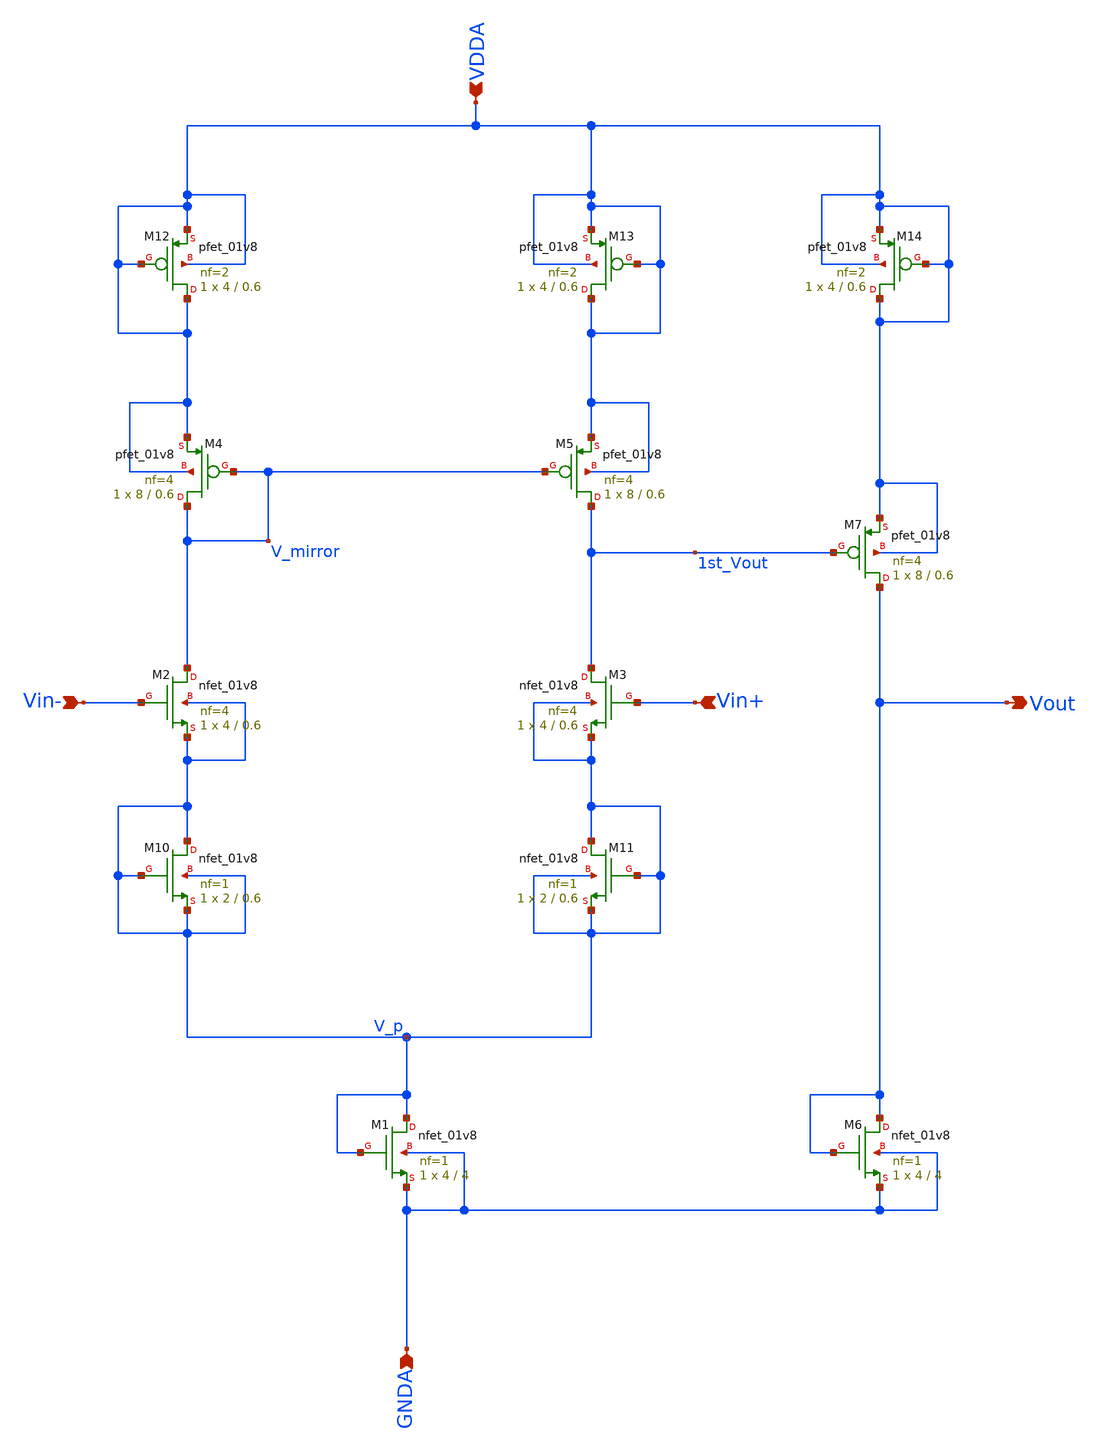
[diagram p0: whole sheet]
** sch_path: projects/bandgapref/xschem_ngspice/new_files/opamp_bandgap_dummy.sch
**.subckt opamp_bandgap_dummy Vin+ Vout Vin- GNDA VDDA
*.ipin Vin+
*.opin Vout
*.ipin Vin-
*.ipin GNDA
*.ipin VDDA
XM1 V_p V_p GNDA GNDA sky130_fd_pr__nfet_01v8 L=4 W=4 nf=1 ad='int((nf+1)/2) * W/nf * 0.29' as='int((nf+2)/2) * W/nf * 0.29'
+ pd='2*int((nf+1)/2) * (W/nf + 0.29)' ps='2*int((nf+2)/2) * (W/nf + 0.29)' nrd='0.29 / W' nrs='0.29 / W'
+ sa=0 sb=0 sd=0 mult=1 m=1
XM2 V_mirror Vin- V_p V_p sky130_fd_pr__nfet_01v8 L=0.6 W=4 nf=4 ad='int((nf+1)/2) * W/nf * 0.29' as='int((nf+2)/2) * W/nf * 0.29'
+ pd='2*int((nf+1)/2) * (W/nf + 0.29)' ps='2*int((nf+2)/2) * (W/nf + 0.29)' nrd='0.29 / W' nrs='0.29 / W'
+ sa=0 sb=0 sd=0 mult=1 m=1
XM3 1st_Vout Vin+ V_p V_p sky130_fd_pr__nfet_01v8 L=0.6 W=4 nf=4 ad='int((nf+1)/2) * W/nf * 0.29' as='int((nf+2)/2) * W/nf * 0.29'
+ pd='2*int((nf+1)/2) * (W/nf + 0.29)' ps='2*int((nf+2)/2) * (W/nf + 0.29)' nrd='0.29 / W' nrs='0.29 / W'
+ sa=0 sb=0 sd=0 mult=1 m=1
XM4 V_mirror V_mirror VDDA VDDA sky130_fd_pr__pfet_01v8 L=0.6 W=8 nf=4 ad='int((nf+1)/2) * W/nf * 0.29'
+ as='int((nf+2)/2) * W/nf * 0.29' pd='2*int((nf+1)/2) * (W/nf + 0.29)' ps='2*int((nf+2)/2) * (W/nf + 0.29)'
+ nrd='0.29 / W' nrs='0.29 / W' sa=0 sb=0 sd=0 mult=1 m=1
XM5 1st_Vout V_mirror VDDA VDDA sky130_fd_pr__pfet_01v8 L=0.6 W=8 nf=4 ad='int((nf+1)/2) * W/nf * 0.29'
+ as='int((nf+2)/2) * W/nf * 0.29' pd='2*int((nf+1)/2) * (W/nf + 0.29)' ps='2*int((nf+2)/2) * (W/nf + 0.29)'
+ nrd='0.29 / W' nrs='0.29 / W' sa=0 sb=0 sd=0 mult=1 m=1
XM6 Vout Vout GNDA GNDA sky130_fd_pr__nfet_01v8 L=4 W=4 nf=1 ad='int((nf+1)/2) * W/nf * 0.29' as='int((nf+2)/2) * W/nf * 0.29'
+ pd='2*int((nf+1)/2) * (W/nf + 0.29)' ps='2*int((nf+2)/2) * (W/nf + 0.29)' nrd='0.29 / W' nrs='0.29 / W'
+ sa=0 sb=0 sd=0 mult=1 m=1
XM7 Vout 1st_Vout VDDA VDDA sky130_fd_pr__pfet_01v8 L=0.6 W=8 nf=4 ad='int((nf+1)/2) * W/nf * 0.29' as='int((nf+2)/2) * W/nf * 0.29'
+ pd='2*int((nf+1)/2) * (W/nf + 0.29)' ps='2*int((nf+2)/2) * (W/nf + 0.29)' nrd='0.29 / W' nrs='0.29 / W'
+ sa=0 sb=0 sd=0 mult=1 m=1
XM10 V_p V_p V_p V_p sky130_fd_pr__nfet_01v8 L=0.6 W=2 nf=1 ad='int((nf+1)/2) * W/nf * 0.29' as='int((nf+2)/2) * W/nf * 0.29'
+ pd='2*int((nf+1)/2) * (W/nf + 0.29)' ps='2*int((nf+2)/2) * (W/nf + 0.29)' nrd='0.29 / W' nrs='0.29 / W'
+ sa=0 sb=0 sd=0 mult=1 m=1
XM11 V_p V_p V_p V_p sky130_fd_pr__nfet_01v8 L=0.6 W=2 nf=1 ad='int((nf+1)/2) * W/nf * 0.29' as='int((nf+2)/2) * W/nf * 0.29'
+ pd='2*int((nf+1)/2) * (W/nf + 0.29)' ps='2*int((nf+2)/2) * (W/nf + 0.29)' nrd='0.29 / W' nrs='0.29 / W'
+ sa=0 sb=0 sd=0 mult=1 m=1
XM12 VDDA VDDA VDDA VDDA sky130_fd_pr__pfet_01v8 L=0.6 W=4 nf=2 ad='int((nf+1)/2) * W/nf * 0.29' as='int((nf+2)/2) * W/nf * 0.29'
+ pd='2*int((nf+1)/2) * (W/nf + 0.29)' ps='2*int((nf+2)/2) * (W/nf + 0.29)' nrd='0.29 / W' nrs='0.29 / W'
+ sa=0 sb=0 sd=0 mult=1 m=1
XM13 VDDA VDDA VDDA VDDA sky130_fd_pr__pfet_01v8 L=0.6 W=4 nf=2 ad='int((nf+1)/2) * W/nf * 0.29' as='int((nf+2)/2) * W/nf * 0.29'
+ pd='2*int((nf+1)/2) * (W/nf + 0.29)' ps='2*int((nf+2)/2) * (W/nf + 0.29)' nrd='0.29 / W' nrs='0.29 / W'
+ sa=0 sb=0 sd=0 mult=1 m=1
XM14 VDDA VDDA VDDA VDDA sky130_fd_pr__pfet_01v8 L=0.6 W=4 nf=2 ad='int((nf+1)/2) * W/nf * 0.29' as='int((nf+2)/2) * W/nf * 0.29'
+ pd='2*int((nf+1)/2) * (W/nf + 0.29)' ps='2*int((nf+2)/2) * (W/nf + 0.29)' nrd='0.29 / W' nrs='0.29 / W'
+ sa=0 sb=0 sd=0 mult=1 m=1
**.ends
.end
